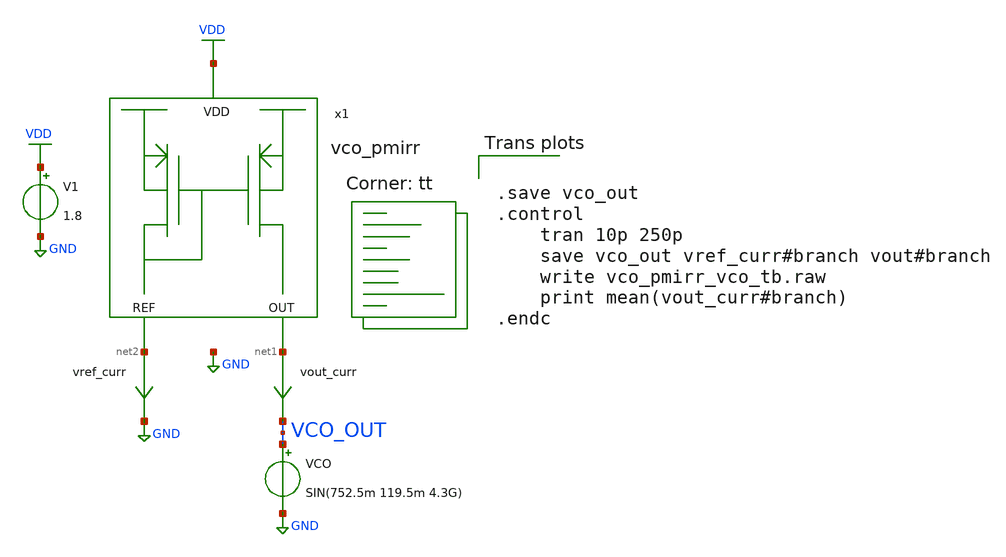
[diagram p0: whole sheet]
** sch_path: xschem/vco/testbenches/vco_pmirr/vco_pmirr_vco_tb.sch
* YI/C9Shc8z/CWPKLJb8BQD+O4ziO4wpAwbu7u7s7HEAy2IIt2IIlQD6O4ziO4ypAAICtDl/GPL8AgNZy7Go7vwAAAAAAAAAAAAAAAAAAAAAAAPeMn2NHvywNosQhFFq
**.subckt vco_pmirr_vco_tb
x1 VDD net1 net2 vco_pmirr
vout_curr net1 VCO_OUT 0
.save i(vout_curr)
V1 VDD GND 1.8
vref_curr net2 GND 0
.save i(vref_curr)
VCO VCO_OUT GND SIN(752.5m 119.5m 4.3G)
**** begin user architecture code
.lib $::SKYWATER_MODELS/sky130.lib.spice tt


.save vco_out
.control
    tran 10p 250p
    save vco_out vref_curr#branch vout#branch
    write vco_pmirr_vco_tb.raw
    print mean(vout_curr#branch)
.endc


**** end user architecture code
**.ends
.GLOBAL GND
.GLOBAL VDD
.end
